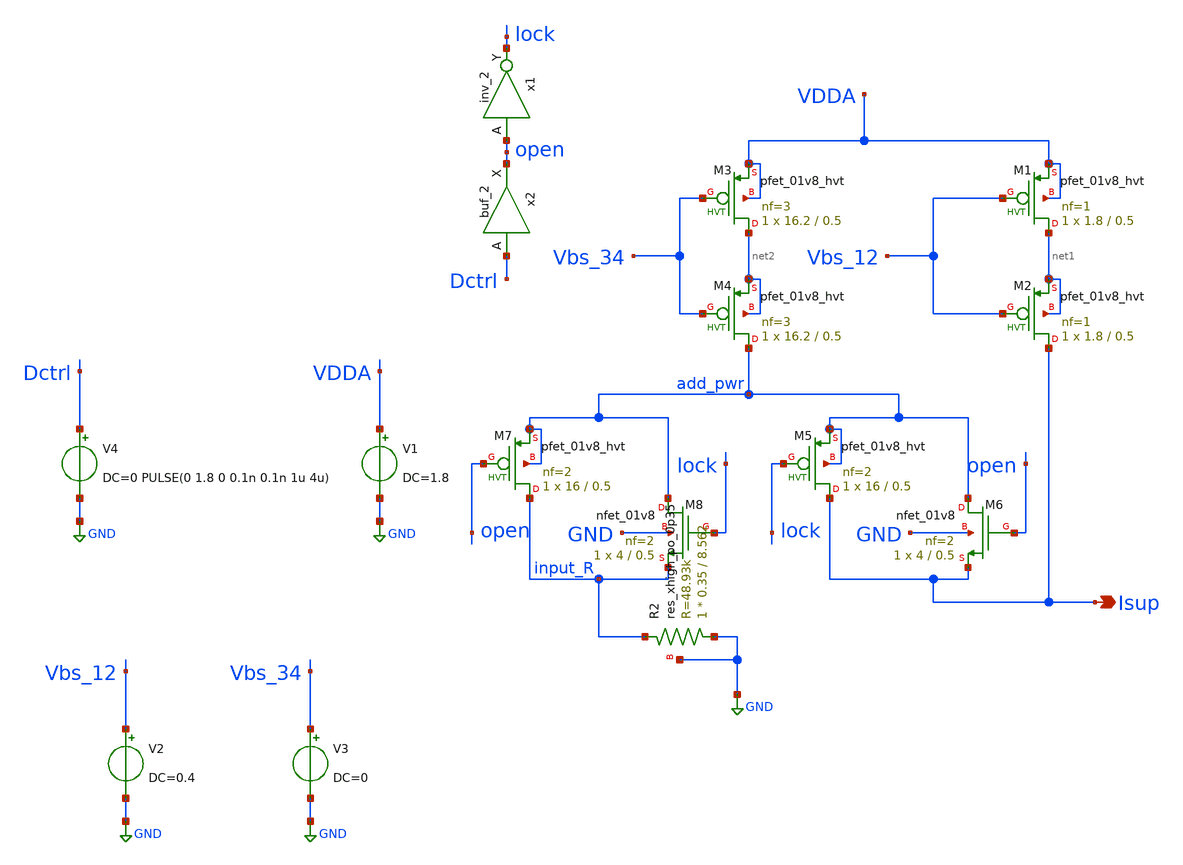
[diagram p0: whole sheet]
** sch_path: xschem/tb/ALib_IDAC_tb.sch
**.subckt ALib_IDAC_tb Isup
*.opin Isup
x1 open GND GND VDDA VDDA lock sky130_fd_sc_hd__inv_2
XM1 net1 Vbs_12 VDDA VDDA sky130_fd_pr__pfet_01v8_hvt L=0.5 W=1.8 nf=1 ad='int((1 + 1)/2) * 1.8 / 1 * 0.29'
+ as='int((1 + 2)/2) * 1.8 / 1 * 0.29' pd='2*int((1 + 1)/2) * (1.8 / 1 + 0.29)' ps='2*int((1 + 2)/2) * (1.8 / 1 + 0.29)'
+ nrd='0.29 / 1.8 ' nrs='0.29 / 1.8 ' sa=0 sb=0 sd=0 mult=1 m=1
XM2 Isup Vbs_12 net1 net1 sky130_fd_pr__pfet_01v8_hvt L=0.5 W=1.8 nf=1 ad='int((1 + 1)/2) * 1.8 / 1 * 0.29'
+ as='int((1 + 2)/2) * 1.8 / 1 * 0.29' pd='2*int((1 + 1)/2) * (1.8 / 1 + 0.29)' ps='2*int((1 + 2)/2) * (1.8 / 1 + 0.29)'
+ nrd='0.29 / 1.8 ' nrs='0.29 / 1.8 ' sa=0 sb=0 sd=0 mult=1 m=1
x2 Dctrl GND GND VDDA VDDA open sky130_fd_sc_hd__buf_2
XM3 net2 Vbs_34 VDDA VDDA sky130_fd_pr__pfet_01v8_hvt L=0.5 W=16.2 nf=3 ad='int((3 + 1)/2) * 16.2 / 3 * 0.29'
+ as='int((3 + 2)/2) * 16.2 / 3 * 0.29' pd='2*int((3 + 1)/2) * (16.2 / 3 + 0.29)' ps='2*int((3 + 2)/2) * (16.2 / 3 + 0.29)'
+ nrd='0.29 / 16.2 ' nrs='0.29 / 16.2 ' sa=0 sb=0 sd=0 mult=1 m=1
XM4 add_pwr Vbs_34 net2 net2 sky130_fd_pr__pfet_01v8_hvt L=0.5 W=16.2 nf=3 ad='int((3 + 1)/2) * 16.2 / 3 * 0.29'
+ as='int((3 + 2)/2) * 16.2 / 3 * 0.29' pd='2*int((3 + 1)/2) * (16.2 / 3 + 0.29)' ps='2*int((3 + 2)/2) * (16.2 / 3 + 0.29)'
+ nrd='0.29 / 16.2 ' nrs='0.29 / 16.2 ' sa=0 sb=0 sd=0 mult=1 m=1
XM5 Isup lock add_pwr add_pwr sky130_fd_pr__pfet_01v8_hvt L=0.5 W=16 nf=2 ad='int((2 + 1)/2) * 16 / 2 * 0.29'
+ as='int((2 + 2)/2) * 16 / 2 * 0.29' pd='2*int((2 + 1)/2) * (16 / 2 + 0.29)' ps='2*int((2 + 2)/2) * (16 / 2 + 0.29)'
+ nrd='0.29 / 16 ' nrs='0.29 / 16 ' sa=0 sb=0 sd=0 mult=1 m=1
XM6 add_pwr open Isup GND sky130_fd_pr__nfet_01v8 L=0.5 W=4 nf=2 ad='int((2 + 1)/2) * 4 / 2 * 0.29' as='int((2 + 2)/2) * 4 / 2 * 0.29'
+ pd='2*int((2 + 1)/2) * (4 / 2 + 0.29)' ps='2*int((2 + 2)/2) * (4 / 2 + 0.29)' nrd='0.29 / 4 ' nrs='0.29 / 4 '
+ sa=0 sb=0 sd=0 mult=1 m=1
XM7 input_R open add_pwr add_pwr sky130_fd_pr__pfet_01v8_hvt L=0.5 W=16 nf=2 ad='int((2 + 1)/2) * 16 / 2 * 0.29'
+ as='int((2 + 2)/2) * 16 / 2 * 0.29' pd='2*int((2 + 1)/2) * (16 / 2 + 0.29)' ps='2*int((2 + 2)/2) * (16 / 2 + 0.29)'
+ nrd='0.29 / 16 ' nrs='0.29 / 16 ' sa=0 sb=0 sd=0 mult=1 m=1
XM8 add_pwr lock input_R GND sky130_fd_pr__nfet_01v8 L=0.5 W=4 nf=2 ad='int((2 + 1)/2) * 4 / 2 * 0.29'
+ as='int((2 + 2)/2) * 4 / 2 * 0.29' pd='2*int((2 + 1)/2) * (4 / 2 + 0.29)' ps='2*int((2 + 2)/2) * (4 / 2 + 0.29)'
+ nrd='0.29 / 4 ' nrs='0.29 / 4 ' sa=0 sb=0 sd=0 mult=1 m=1
XR2 GND input_R GND sky130_fd_pr__res_xhigh_po_0p35 L=8.562 mult=1 m=1
V1 VDDA GND DC=1.8
V2 Vbs_12 GND DC=0.4
V3 Vbs_34 GND DC=0
V4 Dctrl GND DC=0 PULSE(0 1.8 0 0.1n 0.1n 1u 4u)
**** begin user architecture code


.lib /home/dkits/openpdks/sky130A/libs.tech/ngspice/sky130.lib.spice tt
.inc /home/dkits/openpdks/sky130A/libs.ref/sky130_fd_sc_hd/spice/sky130_fd_sc_hd.spice




.control
set num_threads=10
save all
TRAN 1n 50u $ start=0
.endc


**** end user architecture code
**.ends
.GLOBAL GND
.end
